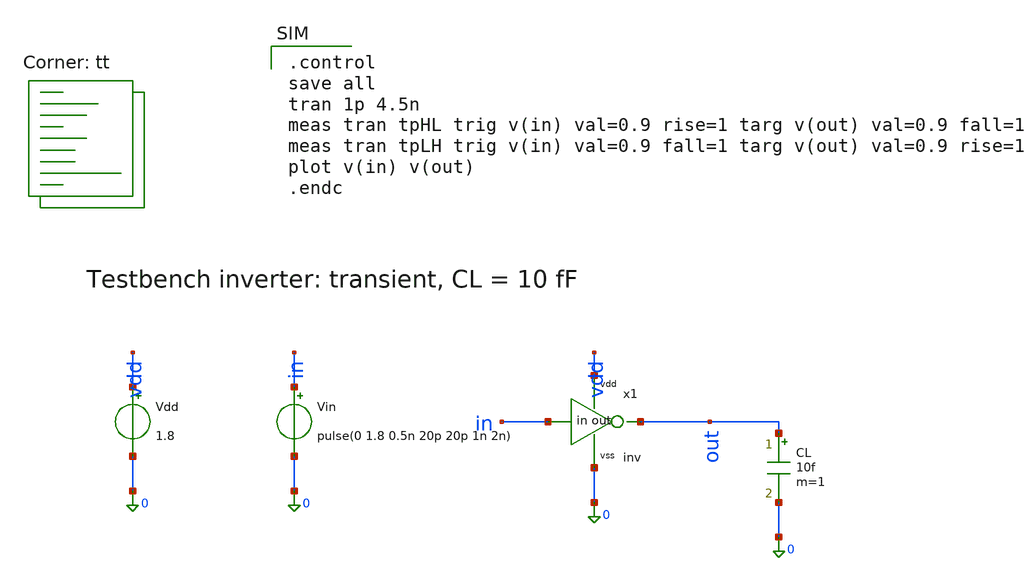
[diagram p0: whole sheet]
** sch_path: lab3/xschem/tb_inv.sch
**.subckt tb_inv
Vdd vdd 0 1.8
.save i(vdd)
Vin in 0 pulse(0 1.8 0.5n 20p 20p 1n 2n)
.save i(vin)
x1 in out vdd 0 inv
CL out 0 10f m=1
**** begin user architecture code
.lib $::SKYWATER_MODELS/sky130.lib.spice tt

.control
save all
tran 1p 4.5n
meas tran tpHL trig v(in) val=0.9 rise=1 targ v(out) val=0.9 fall=1
meas tran tpLH trig v(in) val=0.9 fall=1 targ v(out) val=0.9 rise=1
plot v(in) v(out)
.endc

**** end user architecture code
**.ends
.end
